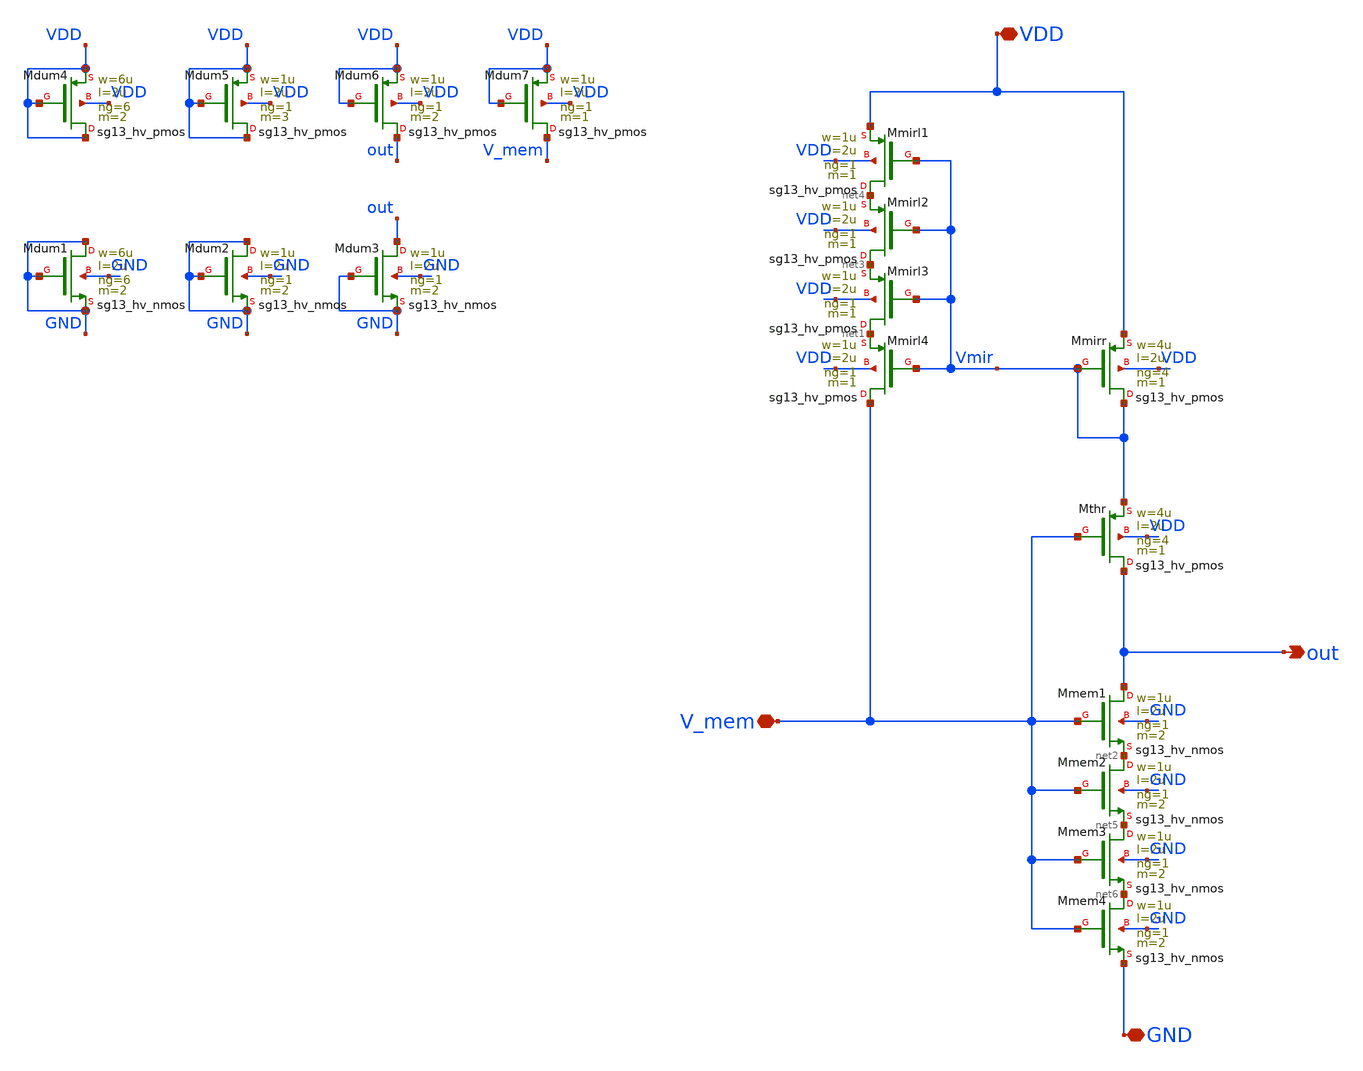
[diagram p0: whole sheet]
** sch_path: xschem/FB_system.sch
**.subckt FB_system out V_mem VDD GND
*.opin out
*.iopin V_mem
*.iopin VDD
*.iopin GND
XMmirr Vmir Vmir VDD VDD sg13_hv_pmos w=4u l=2u ng=4 m=1 mm_ok=1
XMmirl4 V_mem Vmir net1 VDD sg13_hv_pmos w=1u l=2u ng=1 m=1 mm_ok=1
XMthr out V_mem Vmir VDD sg13_hv_pmos w=4u l=2u ng=4 m=1 mm_ok=1
XMmem1 out V_mem net2 GND sg13_hv_nmos w=1u l=2u ng=1 m=2 mm_ok=1
XMmirl3 net1 Vmir net3 VDD sg13_hv_pmos w=1u l=2u ng=1 m=1 mm_ok=1
XMmirl2 net3 Vmir net4 VDD sg13_hv_pmos w=1u l=2u ng=1 m=1 mm_ok=1
XMmirl1 net4 Vmir VDD VDD sg13_hv_pmos w=1u l=2u ng=1 m=1 mm_ok=1
XMmem2 net2 V_mem net5 GND sg13_hv_nmos w=1u l=2u ng=1 m=2 mm_ok=1
XMmem3 net5 V_mem net6 GND sg13_hv_nmos w=1u l=2u ng=1 m=2 mm_ok=1
XMmem4 net6 V_mem GND GND sg13_hv_nmos w=1u l=2u ng=1 m=2 mm_ok=1
XMdum1 GND GND GND GND sg13_hv_nmos w=6u l=2u ng=6 m=2 mm_ok=1
XMdum2 GND GND GND GND sg13_hv_nmos w=1u l=2u ng=1 m=2 mm_ok=1
XMdum3 out GND GND GND sg13_hv_nmos w=1u l=2u ng=1 m=2 mm_ok=1
XMdum4 VDD VDD VDD VDD sg13_hv_pmos w=6u l=2u ng=6 m=2 mm_ok=1
XMdum5 VDD VDD VDD VDD sg13_hv_pmos w=1u l=2u ng=1 m=3 mm_ok=1
XMdum6 out VDD VDD VDD sg13_hv_pmos w=1u l=2u ng=1 m=2 mm_ok=1
XMdum7 V_mem VDD VDD VDD sg13_hv_pmos w=1u l=2u ng=1 m=1 mm_ok=1
**.ends
.end
